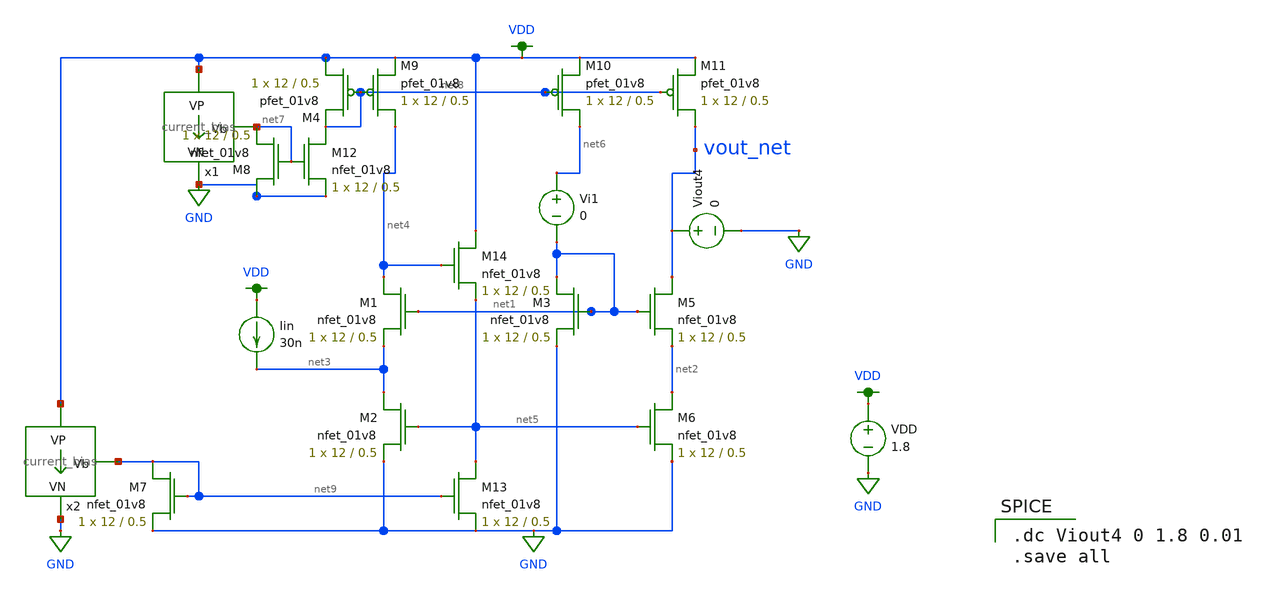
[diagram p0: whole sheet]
** sch_path: Final DAC files/current mirrors/low_voltage_flipped_voltage follower_current_mirror_2.sch
**.subckt low_voltage_flipped_voltage follower_current_mirror_2
XM1 net4 net1 net3 GND sky130_fd_pr__nfet_01v8 L=0.5 W=12 nf=1 ad='int((nf+1)/2) * W/nf * 0.29' as='int((nf+2)/2) * W/nf * 0.29'
+ pd='2*int((nf+1)/2) * (W/nf + 0.29)' ps='2*int((nf+2)/2) * (W/nf + 0.29)' nrd='0.29 / W' nrs='0.29 / W'
+ sa=0 sb=0 sd=0 mult=1 m=1
XM2 net3 net5 GND GND sky130_fd_pr__nfet_01v8 L=0.5 W=12 nf=1 ad='int((nf+1)/2) * W/nf * 0.29' as='int((nf+2)/2) * W/nf * 0.29'
+ pd='2*int((nf+1)/2) * (W/nf + 0.29)' ps='2*int((nf+2)/2) * (W/nf + 0.29)' nrd='0.29 / W' nrs='0.29 / W'
+ sa=0 sb=0 sd=0 mult=1 m=1
XM3 net1 net1 GND GND sky130_fd_pr__nfet_01v8 L=0.5 W=12 nf=1 ad='int((nf+1)/2) * W/nf * 0.29' as='int((nf+2)/2) * W/nf * 0.29'
+ pd='2*int((nf+1)/2) * (W/nf + 0.29)' ps='2*int((nf+2)/2) * (W/nf + 0.29)' nrd='0.29 / W' nrs='0.29 / W'
+ sa=0 sb=0 sd=0 mult=1 m=1
XM5 vout_net net1 net2 GND sky130_fd_pr__nfet_01v8 L=0.5 W=12 nf=1 ad='int((nf+1)/2) * W/nf * 0.29' as='int((nf+2)/2) * W/nf * 0.29'
+ pd='2*int((nf+1)/2) * (W/nf + 0.29)' ps='2*int((nf+2)/2) * (W/nf + 0.29)' nrd='0.29 / W' nrs='0.29 / W'
+ sa=0 sb=0 sd=0 mult=1 m=1
XM6 net2 net5 GND GND sky130_fd_pr__nfet_01v8 L=0.5 W=12 nf=1 ad='int((nf+1)/2) * W/nf * 0.29' as='int((nf+2)/2) * W/nf * 0.29'
+ pd='2*int((nf+1)/2) * (W/nf + 0.29)' ps='2*int((nf+2)/2) * (W/nf + 0.29)' nrd='0.29 / W' nrs='0.29 / W'
+ sa=0 sb=0 sd=0 mult=1 m=1
Viout4 vout_net GND 0
Iin VDD net3 30n
VDD VDD GND 1.8
x1 VDD net7 GND current_bias
XM8 GND net7 net7 GND sky130_fd_pr__nfet_01v8 L=0.5 W=12 nf=1 ad='int((nf+1)/2) * W/nf * 0.29' as='int((nf+2)/2) * W/nf * 0.29'
+ pd='2*int((nf+1)/2) * (W/nf + 0.29)' ps='2*int((nf+2)/2) * (W/nf + 0.29)' nrd='0.29 / W' nrs='0.29 / W'
+ sa=0 sb=0 sd=0 mult=1 m=1
Vi1 net6 net1 0
XM4 VDD net8 net8 VDD sky130_fd_pr__pfet_01v8 L=0.5 W=12 nf=1 ad='int((nf+1)/2) * W/nf * 0.29' as='int((nf+2)/2) * W/nf * 0.29'
+ pd='2*int((nf+1)/2) * (W/nf + 0.29)' ps='2*int((nf+2)/2) * (W/nf + 0.29)' nrd='0.29 / W' nrs='0.29 / W'
+ sa=0 sb=0 sd=0 mult=1 m=1
XM9 net4 net8 VDD VDD sky130_fd_pr__pfet_01v8 L=0.5 W=12 nf=1 ad='int((nf+1)/2) * W/nf * 0.29' as='int((nf+2)/2) * W/nf * 0.29'
+ pd='2*int((nf+1)/2) * (W/nf + 0.29)' ps='2*int((nf+2)/2) * (W/nf + 0.29)' nrd='0.29 / W' nrs='0.29 / W'
+ sa=0 sb=0 sd=0 mult=1 m=1
XM10 net6 net8 VDD VDD sky130_fd_pr__pfet_01v8 L=0.5 W=12 nf=1 ad='int((nf+1)/2) * W/nf * 0.29' as='int((nf+2)/2) * W/nf * 0.29'
+ pd='2*int((nf+1)/2) * (W/nf + 0.29)' ps='2*int((nf+2)/2) * (W/nf + 0.29)' nrd='0.29 / W' nrs='0.29 / W'
+ sa=0 sb=0 sd=0 mult=1 m=1
XM11 vout_net net8 VDD VDD sky130_fd_pr__pfet_01v8 L=0.5 W=12 nf=1 ad='int((nf+1)/2) * W/nf * 0.29' as='int((nf+2)/2) * W/nf * 0.29'
+ pd='2*int((nf+1)/2) * (W/nf + 0.29)' ps='2*int((nf+2)/2) * (W/nf + 0.29)' nrd='0.29 / W' nrs='0.29 / W'
+ sa=0 sb=0 sd=0 mult=1 m=1
XM12 net8 net7 GND GND sky130_fd_pr__nfet_01v8 L=0.5 W=12 nf=1 ad='int((nf+1)/2) * W/nf * 0.29' as='int((nf+2)/2) * W/nf * 0.29'
+ pd='2*int((nf+1)/2) * (W/nf + 0.29)' ps='2*int((nf+2)/2) * (W/nf + 0.29)' nrd='0.29 / W' nrs='0.29 / W'
+ sa=0 sb=0 sd=0 mult=1 m=1
XM13 net5 net9 GND GND sky130_fd_pr__nfet_01v8 L=0.5 W=12 nf=1 ad='int((nf+1)/2) * W/nf * 0.29' as='int((nf+2)/2) * W/nf * 0.29'
+ pd='2*int((nf+1)/2) * (W/nf + 0.29)' ps='2*int((nf+2)/2) * (W/nf + 0.29)' nrd='0.29 / W' nrs='0.29 / W'
+ sa=0 sb=0 sd=0 mult=1 m=1
XM14 VDD net4 net5 GND sky130_fd_pr__nfet_01v8 L=0.5 W=12 nf=1 ad='int((nf+1)/2) * W/nf * 0.29' as='int((nf+2)/2) * W/nf * 0.29'
+ pd='2*int((nf+1)/2) * (W/nf + 0.29)' ps='2*int((nf+2)/2) * (W/nf + 0.29)' nrd='0.29 / W' nrs='0.29 / W'
+ sa=0 sb=0 sd=0 mult=1 m=1
x2 VDD net9 GND current_bias
XM7 net9 net9 GND GND sky130_fd_pr__nfet_01v8 L=0.5 W=12 nf=1 ad='int((nf+1)/2) * W/nf * 0.29' as='int((nf+2)/2) * W/nf * 0.29'
+ pd='2*int((nf+1)/2) * (W/nf + 0.29)' ps='2*int((nf+2)/2) * (W/nf + 0.29)' nrd='0.29 / W' nrs='0.29 / W'
+ sa=0 sb=0 sd=0 mult=1 m=1
**** begin user architecture code

.option wnflag=1
.param MC_SWITCH=0.0
.lib ~/skywater/skywater-pdk/libraries/sky130_fd_pr_ngspice/latest/models/sky130.lib.spice tt


.dc Viout4 0 1.8 0.01
.save all

**** end user architecture code
**.ends
.GLOBAL GND
.GLOBAL VDD
.end
